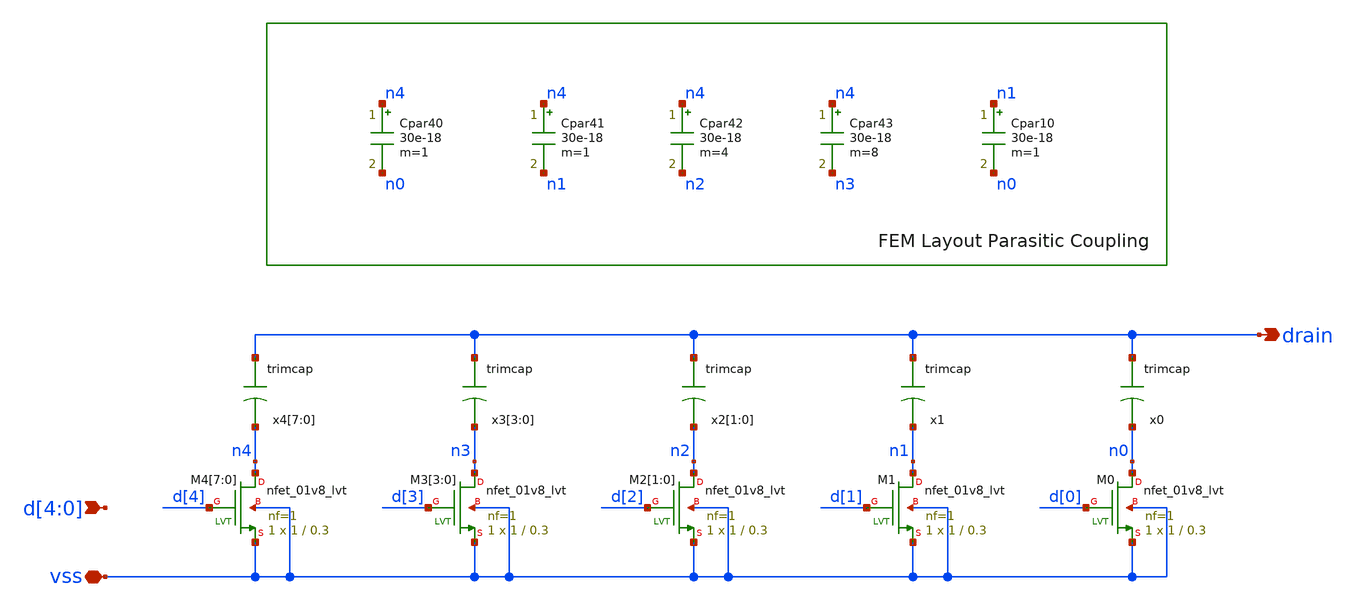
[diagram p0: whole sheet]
** sch_path: xschem/sar_10b/comparator/trim.sch
**.subckt trim vss d[4],d[3],d[2],d[1],d[0] drain
*.iopin vss
*.ipin d[4],d[3],d[2],d[1],d[0]
*.opin drain
XM4[7] n4 d[4] vss vss sky130_fd_pr__nfet_01v8_lvt L=0.3 W=1 nf=1 ad='int((nf+1)/2) * W/nf * 0.29' as='int((nf+2)/2) * W/nf * 0.29'
+ pd='2*int((nf+1)/2) * (W/nf + 0.29)' ps='2*int((nf+2)/2) * (W/nf + 0.29)' nrd='0.29 / W' nrs='0.29 / W'
+ sa=0 sb=0 sd=0 mult=1 m=1
XM4[6] n4 d[4] vss vss sky130_fd_pr__nfet_01v8_lvt L=0.3 W=1 nf=1 ad='int((nf+1)/2) * W/nf * 0.29' as='int((nf+2)/2) * W/nf * 0.29'
+ pd='2*int((nf+1)/2) * (W/nf + 0.29)' ps='2*int((nf+2)/2) * (W/nf + 0.29)' nrd='0.29 / W' nrs='0.29 / W'
+ sa=0 sb=0 sd=0 mult=1 m=1
XM4[5] n4 d[4] vss vss sky130_fd_pr__nfet_01v8_lvt L=0.3 W=1 nf=1 ad='int((nf+1)/2) * W/nf * 0.29' as='int((nf+2)/2) * W/nf * 0.29'
+ pd='2*int((nf+1)/2) * (W/nf + 0.29)' ps='2*int((nf+2)/2) * (W/nf + 0.29)' nrd='0.29 / W' nrs='0.29 / W'
+ sa=0 sb=0 sd=0 mult=1 m=1
XM4[4] n4 d[4] vss vss sky130_fd_pr__nfet_01v8_lvt L=0.3 W=1 nf=1 ad='int((nf+1)/2) * W/nf * 0.29' as='int((nf+2)/2) * W/nf * 0.29'
+ pd='2*int((nf+1)/2) * (W/nf + 0.29)' ps='2*int((nf+2)/2) * (W/nf + 0.29)' nrd='0.29 / W' nrs='0.29 / W'
+ sa=0 sb=0 sd=0 mult=1 m=1
XM4[3] n4 d[4] vss vss sky130_fd_pr__nfet_01v8_lvt L=0.3 W=1 nf=1 ad='int((nf+1)/2) * W/nf * 0.29' as='int((nf+2)/2) * W/nf * 0.29'
+ pd='2*int((nf+1)/2) * (W/nf + 0.29)' ps='2*int((nf+2)/2) * (W/nf + 0.29)' nrd='0.29 / W' nrs='0.29 / W'
+ sa=0 sb=0 sd=0 mult=1 m=1
XM4[2] n4 d[4] vss vss sky130_fd_pr__nfet_01v8_lvt L=0.3 W=1 nf=1 ad='int((nf+1)/2) * W/nf * 0.29' as='int((nf+2)/2) * W/nf * 0.29'
+ pd='2*int((nf+1)/2) * (W/nf + 0.29)' ps='2*int((nf+2)/2) * (W/nf + 0.29)' nrd='0.29 / W' nrs='0.29 / W'
+ sa=0 sb=0 sd=0 mult=1 m=1
XM4[1] n4 d[4] vss vss sky130_fd_pr__nfet_01v8_lvt L=0.3 W=1 nf=1 ad='int((nf+1)/2) * W/nf * 0.29' as='int((nf+2)/2) * W/nf * 0.29'
+ pd='2*int((nf+1)/2) * (W/nf + 0.29)' ps='2*int((nf+2)/2) * (W/nf + 0.29)' nrd='0.29 / W' nrs='0.29 / W'
+ sa=0 sb=0 sd=0 mult=1 m=1
XM4[0] n4 d[4] vss vss sky130_fd_pr__nfet_01v8_lvt L=0.3 W=1 nf=1 ad='int((nf+1)/2) * W/nf * 0.29' as='int((nf+2)/2) * W/nf * 0.29'
+ pd='2*int((nf+1)/2) * (W/nf + 0.29)' ps='2*int((nf+2)/2) * (W/nf + 0.29)' nrd='0.29 / W' nrs='0.29 / W'
+ sa=0 sb=0 sd=0 mult=1 m=1
XM3[3] n3 d[3] vss vss sky130_fd_pr__nfet_01v8_lvt L=0.3 W=1 nf=1 ad='int((nf+1)/2) * W/nf * 0.29' as='int((nf+2)/2) * W/nf * 0.29'
+ pd='2*int((nf+1)/2) * (W/nf + 0.29)' ps='2*int((nf+2)/2) * (W/nf + 0.29)' nrd='0.29 / W' nrs='0.29 / W'
+ sa=0 sb=0 sd=0 mult=1 m=1
XM3[2] n3 d[3] vss vss sky130_fd_pr__nfet_01v8_lvt L=0.3 W=1 nf=1 ad='int((nf+1)/2) * W/nf * 0.29' as='int((nf+2)/2) * W/nf * 0.29'
+ pd='2*int((nf+1)/2) * (W/nf + 0.29)' ps='2*int((nf+2)/2) * (W/nf + 0.29)' nrd='0.29 / W' nrs='0.29 / W'
+ sa=0 sb=0 sd=0 mult=1 m=1
XM3[1] n3 d[3] vss vss sky130_fd_pr__nfet_01v8_lvt L=0.3 W=1 nf=1 ad='int((nf+1)/2) * W/nf * 0.29' as='int((nf+2)/2) * W/nf * 0.29'
+ pd='2*int((nf+1)/2) * (W/nf + 0.29)' ps='2*int((nf+2)/2) * (W/nf + 0.29)' nrd='0.29 / W' nrs='0.29 / W'
+ sa=0 sb=0 sd=0 mult=1 m=1
XM3[0] n3 d[3] vss vss sky130_fd_pr__nfet_01v8_lvt L=0.3 W=1 nf=1 ad='int((nf+1)/2) * W/nf * 0.29' as='int((nf+2)/2) * W/nf * 0.29'
+ pd='2*int((nf+1)/2) * (W/nf + 0.29)' ps='2*int((nf+2)/2) * (W/nf + 0.29)' nrd='0.29 / W' nrs='0.29 / W'
+ sa=0 sb=0 sd=0 mult=1 m=1
XM2[1] n2 d[2] vss vss sky130_fd_pr__nfet_01v8_lvt L=0.3 W=1 nf=1 ad='int((nf+1)/2) * W/nf * 0.29' as='int((nf+2)/2) * W/nf * 0.29'
+ pd='2*int((nf+1)/2) * (W/nf + 0.29)' ps='2*int((nf+2)/2) * (W/nf + 0.29)' nrd='0.29 / W' nrs='0.29 / W'
+ sa=0 sb=0 sd=0 mult=1 m=1
XM2[0] n2 d[2] vss vss sky130_fd_pr__nfet_01v8_lvt L=0.3 W=1 nf=1 ad='int((nf+1)/2) * W/nf * 0.29' as='int((nf+2)/2) * W/nf * 0.29'
+ pd='2*int((nf+1)/2) * (W/nf + 0.29)' ps='2*int((nf+2)/2) * (W/nf + 0.29)' nrd='0.29 / W' nrs='0.29 / W'
+ sa=0 sb=0 sd=0 mult=1 m=1
XM1 n1 d[1] vss vss sky130_fd_pr__nfet_01v8_lvt L=0.3 W=1 nf=1 ad='int((nf+1)/2) * W/nf * 0.29' as='int((nf+2)/2) * W/nf * 0.29'
+ pd='2*int((nf+1)/2) * (W/nf + 0.29)' ps='2*int((nf+2)/2) * (W/nf + 0.29)' nrd='0.29 / W' nrs='0.29 / W'
+ sa=0 sb=0 sd=0 mult=1 m=1
XM0 n0 d[0] vss vss sky130_fd_pr__nfet_01v8_lvt L=0.3 W=1 nf=1 ad='int((nf+1)/2) * W/nf * 0.29' as='int((nf+2)/2) * W/nf * 0.29'
+ pd='2*int((nf+1)/2) * (W/nf + 0.29)' ps='2*int((nf+2)/2) * (W/nf + 0.29)' nrd='0.29 / W' nrs='0.29 / W'
+ sa=0 sb=0 sd=0 mult=1 m=1
x4[7] drain n4 trimcap
x4[6] drain n4 trimcap
x4[5] drain n4 trimcap
x4[4] drain n4 trimcap
x4[3] drain n4 trimcap
x4[2] drain n4 trimcap
x4[1] drain n4 trimcap
x4[0] drain n4 trimcap
x3[3] drain n3 trimcap
x3[2] drain n3 trimcap
x3[1] drain n3 trimcap
x3[0] drain n3 trimcap
x2[1] drain n2 trimcap
x2[0] drain n2 trimcap
x1 drain n1 trimcap
x0 drain n0 trimcap
Cpar10 n1 n0 30e-18 m=1
Cpar43 n4 n3 30e-18 m=8
Cpar42 n4 n2 30e-18 m=4
Cpar41 n4 n1 30e-18 m=1
Cpar40 n4 n0 30e-18 m=1
**.ends

* expanding   symbol:  sar_10b/comparator/trimcap.sym # of pins=2
** sym_path: xschem/sar_10b/comparator/trimcap.sym
** sch_path: xschem/sar_10b/comparator/trimcap.sch
.subckt trimcap cp cn
*.iopin cp
*.iopin cn
c0 cp cn 1.25f m=1
.ends

.end
